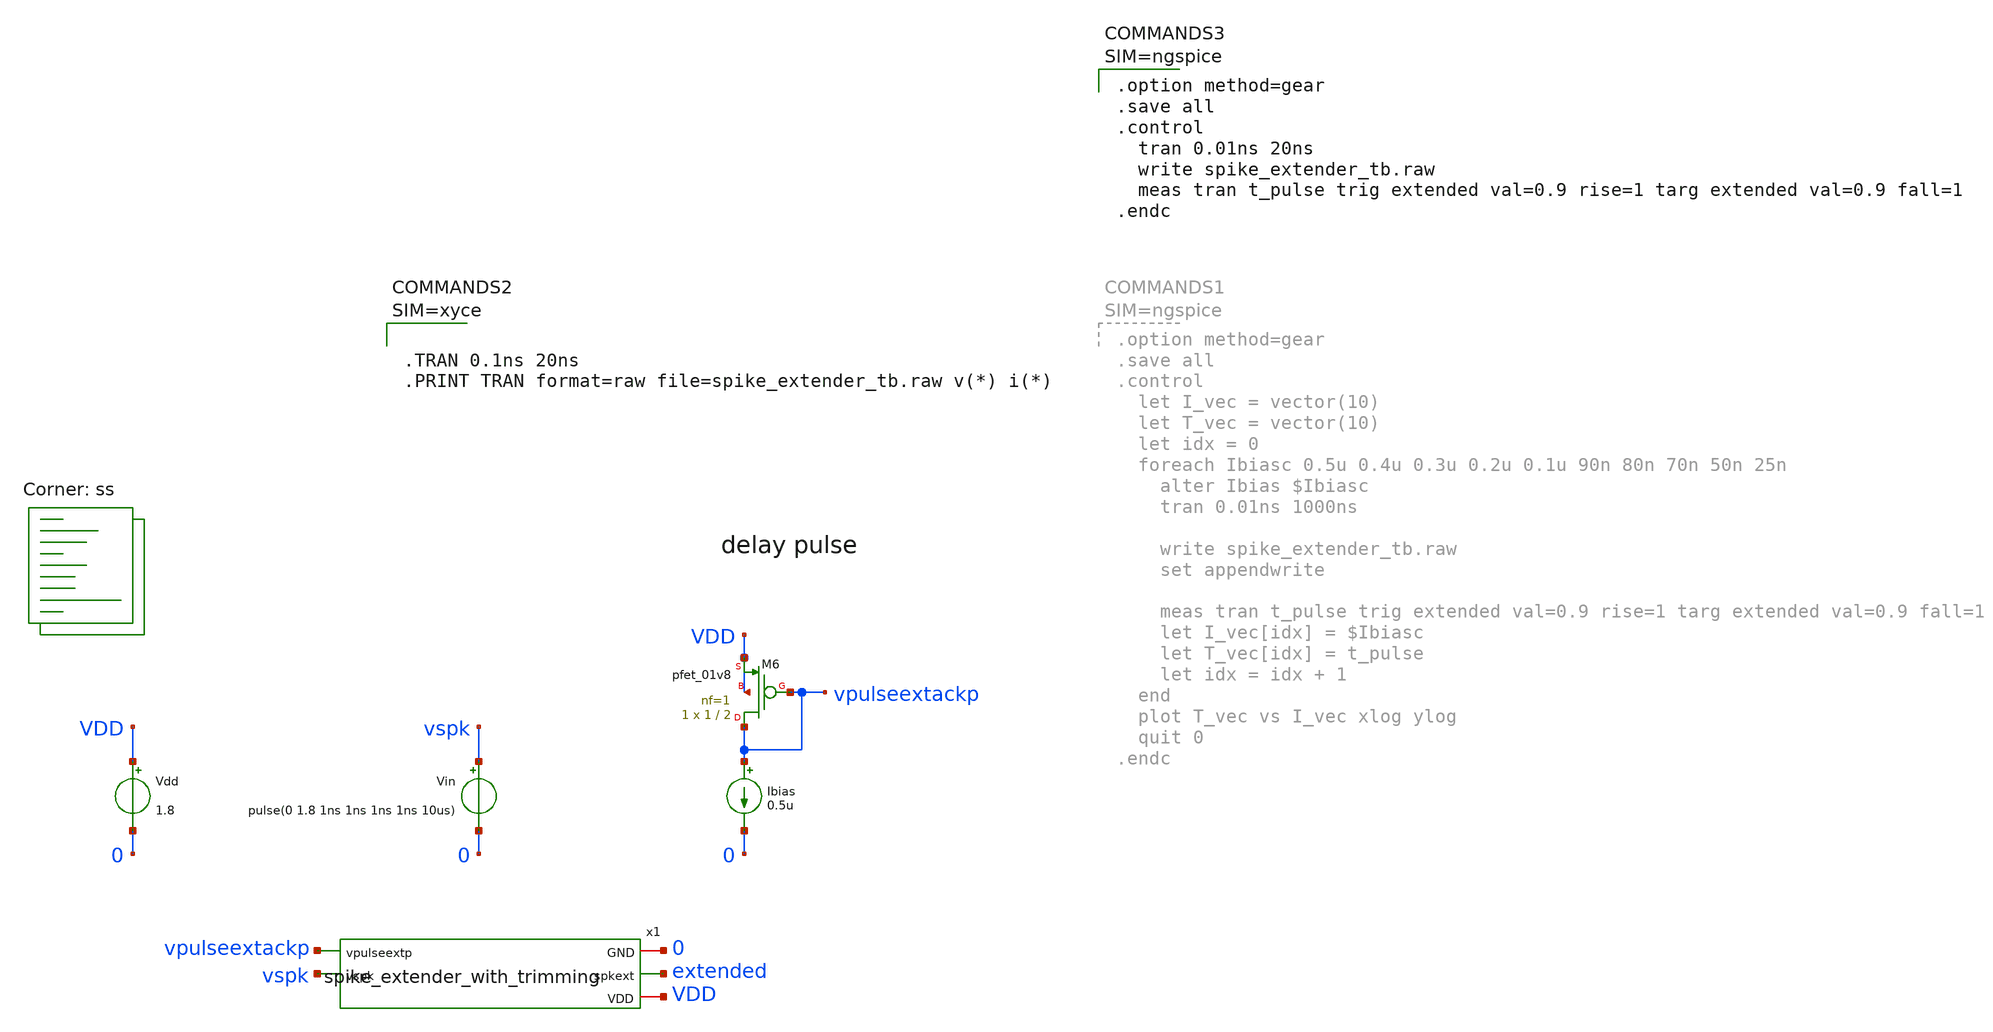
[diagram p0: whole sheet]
** sch_path: design/xschem/spike_extender_tb.sch
**.subckt spike_extender_tb
Vdd VDD 0 1.8
Vin vspk 0 pulse(0 1.8 1ns 1ns 1ns 1ns 10us)
XM6 vpulseextackp vpulseextackp VDD VDD sky130_fd_pr__pfet_01v8 L=2 W=1 nf=1 ad='int((nf+1)/2) * W/nf * 0.29'
+ as='int((nf+2)/2) * W/nf * 0.29' pd='2*int((nf+1)/2) * (W/nf + 0.29)' ps='2*int((nf+2)/2) * (W/nf + 0.29)'
+ nrd='0.29 / W' nrs='0.29 / W' sa=0 sb=0 sd=0 mult=1 m=1
Ibias vpulseextackp 0 0.5u
x1 vpulseextackp vspk 0 extended VDD spike_extender_with_trimming
**** begin user architecture code


* Standard cell simulation files
.include $::SKYWATER_STDCELLS/sky130_fd_sc_hd.spice

* Power domains
VSTDCELL_PWR VPWR 0 DC 1.8
VSTDCELL_PB  VPB  0 DC 1.8
VSTDCELL_NB  VNB  0 DC 0
VSTDCELL_GND VGND 0 DC 0
.global VNB VGND VPB VPWR


.lib $::SKYWATER_MODELS/sky130.lib.spice ss





.option method=gear
.save all
.control
  tran 0.01ns 20ns
  write spike_extender_tb.raw
  meas tran t_pulse trig extended val=0.9 rise=1 targ extended val=0.9 fall=1
.endc



**** end user architecture code
**.ends

* expanding   symbol:  spike_extender_with_trimming.sym # of pins=5
** sym_path: design/xschem/spike_extender_with_trimming.sym
** sch_path: design/xschem/spike_extender_with_trimming.sch
.subckt spike_extender_with_trimming vpulseextp vspk GND spkext VDD
*.iopin GND
*.iopin VDD
*.ipin vspk
*.opin spkext
*.ipin vpulseextp
x1 vpulseextp vpulseshort GND spkext VDD spike_extender
x3 vspk GND GND VDD VDD net1 sky130_fd_sc_hd__clkdlybuf4s50_1
x2 net1 vspk GND GND VDD VDD vpulseshort sky130_fd_sc_hd__nor2b_1
.ends


* expanding   symbol:  spike_extender.sym # of pins=5
** sym_path: design/xschem/spike_extender.sym
** sch_path: design/xschem/spike_extender.sch
.subckt spike_extender vpulseextp spk GND spkext VDD
*.iopin GND
*.iopin VDD
*.ipin spk
*.opin spkext
*.ipin vpulseextp
XM1 net1 spk GND GND sky130_fd_pr__nfet_01v8 L=0.15 W=0.65 nf=1 ad='int((nf+1)/2) * W/nf * 0.29' as='int((nf+2)/2) * W/nf * 0.29'
+ pd='2*int((nf+1)/2) * (W/nf + 0.29)' ps='2*int((nf+2)/2) * (W/nf + 0.29)' nrd='0.29 / W' nrs='0.29 / W'
+ sa=0 sb=0 sd=0 mult=1 m=1
XM6 net1 vpulseextp VDD VDD sky130_fd_pr__pfet_01v8 L=2 W=1 nf=1 ad='int((nf+1)/2) * W/nf * 0.29' as='int((nf+2)/2) * W/nf * 0.29'
+ pd='2*int((nf+1)/2) * (W/nf + 0.29)' ps='2*int((nf+2)/2) * (W/nf + 0.29)' nrd='0.29 / W' nrs='0.29 / W'
+ sa=0 sb=0 sd=0 mult=1 m=1
XM5 net3 net2 GND GND sky130_fd_pr__nfet_01v8 L=0.15 W=0.65 nf=1 ad='int((nf+1)/2) * W/nf * 0.29' as='int((nf+2)/2) * W/nf * 0.29'
+ pd='2*int((nf+1)/2) * (W/nf + 0.29)' ps='2*int((nf+2)/2) * (W/nf + 0.29)' nrd='0.29 / W' nrs='0.29 / W'
+ sa=0 sb=0 sd=0 mult=1 m=1
XM8 spkext net3 GND GND sky130_fd_pr__nfet_01v8 L=0.15 W=0.65 nf=1 ad='int((nf+1)/2) * W/nf * 0.29' as='int((nf+2)/2) * W/nf * 0.29'
+ pd='2*int((nf+1)/2) * (W/nf + 0.29)' ps='2*int((nf+2)/2) * (W/nf + 0.29)' nrd='0.29 / W' nrs='0.29 / W'
+ sa=0 sb=0 sd=0 mult=1 m=1
XM4 net3 net2 VDD VDD sky130_fd_pr__pfet_01v8 L=0.15 W=1.0 nf=1 ad='int((nf+1)/2) * W/nf * 0.29' as='int((nf+2)/2) * W/nf * 0.29'
+ pd='2*int((nf+1)/2) * (W/nf + 0.29)' ps='2*int((nf+2)/2) * (W/nf + 0.29)' nrd='0.29 / W' nrs='0.29 / W'
+ sa=0 sb=0 sd=0 mult=1 m=1
XM7 spkext net3 VDD VDD sky130_fd_pr__pfet_01v8 L=0.15 W=1.0 nf=1 ad='int((nf+1)/2) * W/nf * 0.29' as='int((nf+2)/2) * W/nf * 0.29'
+ pd='2*int((nf+1)/2) * (W/nf + 0.29)' ps='2*int((nf+2)/2) * (W/nf + 0.29)' nrd='0.29 / W' nrs='0.29 / W'
+ sa=0 sb=0 sd=0 mult=1 m=1
XM2 net2 net1 GND GND sky130_fd_pr__nfet_01v8 L=0.15 W=0.65 nf=1 ad='int((nf+1)/2) * W/nf * 0.29' as='int((nf+2)/2) * W/nf * 0.29'
+ pd='2*int((nf+1)/2) * (W/nf + 0.29)' ps='2*int((nf+2)/2) * (W/nf + 0.29)' nrd='0.29 / W' nrs='0.29 / W'
+ sa=0 sb=0 sd=0 mult=1 m=1
XM3 net2 net1 VDD VDD sky130_fd_pr__pfet_01v8 L=0.15 W=1.0 nf=1 ad='int((nf+1)/2) * W/nf * 0.29' as='int((nf+2)/2) * W/nf * 0.29'
+ pd='2*int((nf+1)/2) * (W/nf + 0.29)' ps='2*int((nf+2)/2) * (W/nf + 0.29)' nrd='0.29 / W' nrs='0.29 / W'
+ sa=0 sb=0 sd=0 mult=1 m=1
XM9 GND net1 GND GND sky130_fd_pr__nfet_01v8 L=1 W=0.65 nf=1 ad='int((nf+1)/2) * W/nf * 0.29' as='int((nf+2)/2) * W/nf * 0.29'
+ pd='2*int((nf+1)/2) * (W/nf + 0.29)' ps='2*int((nf+2)/2) * (W/nf + 0.29)' nrd='0.29 / W' nrs='0.29 / W'
+ sa=0 sb=0 sd=0 mult=1 m=1
.ends

.end
